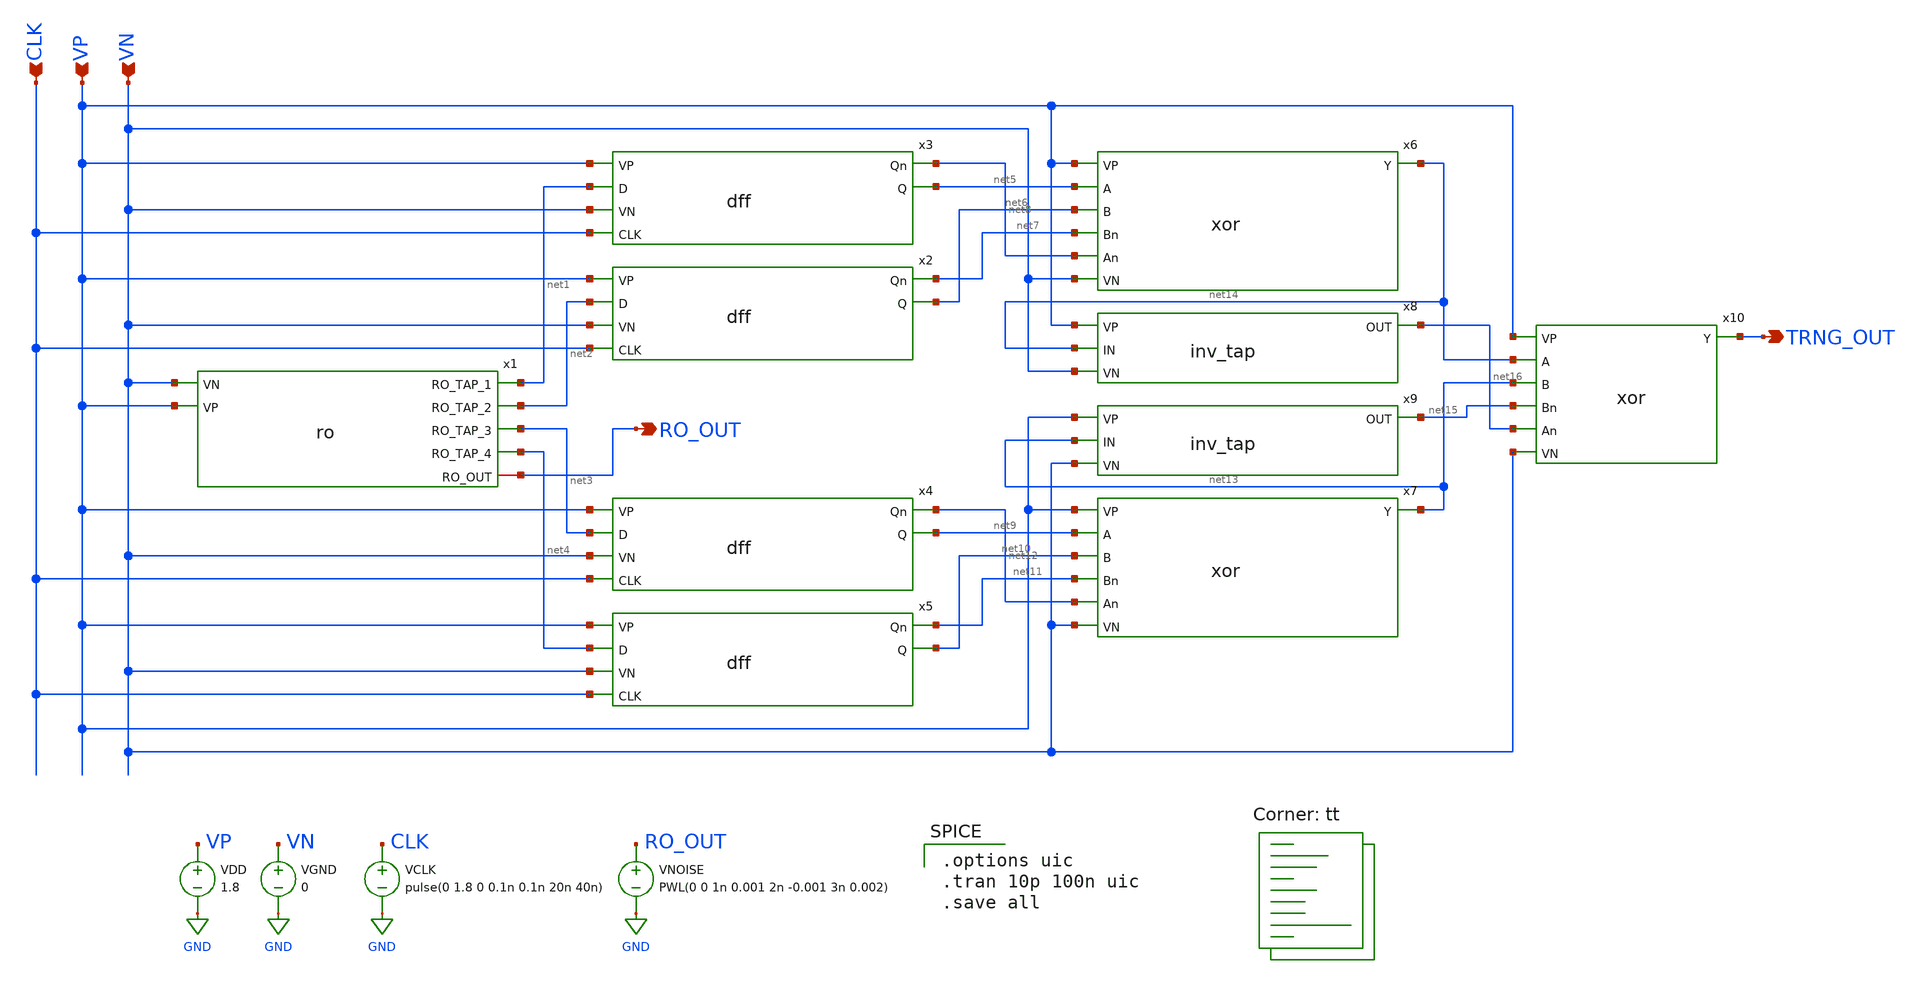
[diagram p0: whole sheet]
** sch_path: Mixed-Signal TRNG/xschem/trng.sch
**.subckt trng VP VN TRNG_OUT CLK RO_OUT
*.ipin VP
*.ipin VN
*.opin TRNG_OUT
*.ipin CLK
*.opin RO_OUT
x2 VP net7 net2 net6 VN CLK dff
x3 VP net8 net1 net5 VN CLK dff
x4 VP net12 net3 net9 VN CLK dff
x5 VP net11 net4 net10 VN CLK dff
x6 VP net5 net6 net14 net7 net8 VN xor
x7 VP net9 net10 net13 net11 net12 VN xor
x8 VP net14 net16 VN inv_tap
x9 VP net13 net15 VN inv_tap
x10 VP net14 net13 TRNG_OUT net15 net16 VN xor
VDD VP GND 1.8
VGND VN GND 0
VCLK CLK GND pulse(0 1.8 0 0.1n 0.1n 20n 40n)
x1 net1 net2 net3 net4 RO_OUT VN VP ro
VNOISE RO_OUT GND PWL(0 0 1n 0.001 2n -0.001 3n 0.002)
**** begin user architecture code

.options uic
.tran 10p 100n uic
.save all

.lib $::SKYWATER_MODELS/sky130.lib.spice tt
**** end user architecture code
**.ends

* expanding   symbol:  /home/madvlsi/Desktop/Mixed-Signal TRNG/xschem/dff.sym # of pins=6
** sym_path: Mixed-Signal TRNG/xschem/dff.sym
** sch_path: Mixed-Signal TRNG/xschem/dff.sch
.subckt dff VP Qn D Q VN CLK
*.opin Qn
*.opin Q
*.ipin D
*.ipin CLK
*.ipin VP
*.ipin VN
XM1 net1 Dn1 VP VP sky130_fd_pr__pfet_01v8 L=0.15 W=2 nf=1 ad='int((nf+1)/2) * W/nf * 0.29' as='int((nf+2)/2) * W/nf * 0.29'
+ pd='2*int((nf+1)/2) * (W/nf + 0.29)' ps='2*int((nf+2)/2) * (W/nf + 0.29)' nrd='0.29 / W' nrs='0.29 / W'
+ sa=0 sb=0 sd=0 mult=1 m=1
XM2 net1 CLK VP VP sky130_fd_pr__pfet_01v8 L=0.15 W=4 nf=1 ad='int((nf+1)/2) * W/nf * 0.29' as='int((nf+2)/2) * W/nf * 0.29'
+ pd='2*int((nf+1)/2) * (W/nf + 0.29)' ps='2*int((nf+2)/2) * (W/nf + 0.29)' nrd='0.29 / W' nrs='0.29 / W'
+ sa=0 sb=0 sd=0 mult=1 m=1
XM3 net7 net10 net1 VP sky130_fd_pr__pfet_01v8 L=0.15 W=2 nf=1 ad='int((nf+1)/2) * W/nf * 0.29' as='int((nf+2)/2) * W/nf * 0.29'
+ pd='2*int((nf+1)/2) * (W/nf + 0.29)' ps='2*int((nf+2)/2) * (W/nf + 0.29)' nrd='0.29 / W' nrs='0.29 / W'
+ sa=0 sb=0 sd=0 mult=1 m=1
XM4 VP D net2 VP sky130_fd_pr__pfet_01v8 L=0.15 W=2 nf=1 ad='int((nf+1)/2) * W/nf * 0.29' as='int((nf+2)/2) * W/nf * 0.29'
+ pd='2*int((nf+1)/2) * (W/nf + 0.29)' ps='2*int((nf+2)/2) * (W/nf + 0.29)' nrd='0.29 / W' nrs='0.29 / W'
+ sa=0 sb=0 sd=0 mult=1 m=1
XM5 net2 CLK VP VP sky130_fd_pr__pfet_01v8 L=0.15 W=4 nf=1 ad='int((nf+1)/2) * W/nf * 0.29' as='int((nf+2)/2) * W/nf * 0.29'
+ pd='2*int((nf+1)/2) * (W/nf + 0.29)' ps='2*int((nf+2)/2) * (W/nf + 0.29)' nrd='0.29 / W' nrs='0.29 / W'
+ sa=0 sb=0 sd=0 mult=1 m=1
XM6 net10 net7 net2 VP sky130_fd_pr__pfet_01v8 L=0.15 W=2 nf=1 ad='int((nf+1)/2) * W/nf * 0.29' as='int((nf+2)/2) * W/nf * 0.29'
+ pd='2*int((nf+1)/2) * (W/nf + 0.29)' ps='2*int((nf+2)/2) * (W/nf + 0.29)' nrd='0.29 / W' nrs='0.29 / W'
+ sa=0 sb=0 sd=0 mult=1 m=1
XM7 VP net7 net3 VP sky130_fd_pr__pfet_01v8 L=0.15 W=2 nf=1 ad='int((nf+1)/2) * W/nf * 0.29' as='int((nf+2)/2) * W/nf * 0.29'
+ pd='2*int((nf+1)/2) * (W/nf + 0.29)' ps='2*int((nf+2)/2) * (W/nf + 0.29)' nrd='0.29 / W' nrs='0.29 / W'
+ sa=0 sb=0 sd=0 mult=1 m=1
XM8 Qn CLK net3 VP sky130_fd_pr__pfet_01v8 L=0.15 W=4 nf=1 ad='int((nf+1)/2) * W/nf * 0.29' as='int((nf+2)/2) * W/nf * 0.29'
+ pd='2*int((nf+1)/2) * (W/nf + 0.29)' ps='2*int((nf+2)/2) * (W/nf + 0.29)' nrd='0.29 / W' nrs='0.29 / W'
+ sa=0 sb=0 sd=0 mult=1 m=1
XM9 VP Q Qn VP sky130_fd_pr__pfet_01v8 L=0.15 W=4 nf=1 ad='int((nf+1)/2) * W/nf * 0.29' as='int((nf+2)/2) * W/nf * 0.29'
+ pd='2*int((nf+1)/2) * (W/nf + 0.29)' ps='2*int((nf+2)/2) * (W/nf + 0.29)' nrd='0.29 / W' nrs='0.29 / W'
+ sa=0 sb=0 sd=0 mult=1 m=1
XM10 net4 net10 VP VP sky130_fd_pr__pfet_01v8 L=0.15 W=2 nf=1 ad='int((nf+1)/2) * W/nf * 0.29' as='int((nf+2)/2) * W/nf * 0.29'
+ pd='2*int((nf+1)/2) * (W/nf + 0.29)' ps='2*int((nf+2)/2) * (W/nf + 0.29)' nrd='0.29 / W' nrs='0.29 / W'
+ sa=0 sb=0 sd=0 mult=1 m=1
XM11 Q CLK net4 VP sky130_fd_pr__pfet_01v8 L=0.15 W=4 nf=1 ad='int((nf+1)/2) * W/nf * 0.29' as='int((nf+2)/2) * W/nf * 0.29'
+ pd='2*int((nf+1)/2) * (W/nf + 0.29)' ps='2*int((nf+2)/2) * (W/nf + 0.29)' nrd='0.29 / W' nrs='0.29 / W'
+ sa=0 sb=0 sd=0 mult=1 m=1
XM12 VP Qn Q VP sky130_fd_pr__pfet_01v8 L=0.15 W=4 nf=1 ad='int((nf+1)/2) * W/nf * 0.29' as='int((nf+2)/2) * W/nf * 0.29'
+ pd='2*int((nf+1)/2) * (W/nf + 0.29)' ps='2*int((nf+2)/2) * (W/nf + 0.29)' nrd='0.29 / W' nrs='0.29 / W'
+ sa=0 sb=0 sd=0 mult=1 m=1
XM13 net9 D VN VN sky130_fd_pr__nfet_01v8 L=0.15 W=1 nf=1 ad='int((nf+1)/2) * W/nf * 0.29' as='int((nf+2)/2) * W/nf * 0.29'
+ pd='2*int((nf+1)/2) * (W/nf + 0.29)' ps='2*int((nf+2)/2) * (W/nf + 0.29)' nrd='0.29 / W' nrs='0.29 / W'
+ sa=0 sb=0 sd=0 mult=1 m=1
XM14 net9 CLK net10 VN sky130_fd_pr__nfet_01v8 L=0.15 W=2 nf=1 ad='int((nf+1)/2) * W/nf * 0.29' as='int((nf+2)/2) * W/nf * 0.29'
+ pd='2*int((nf+1)/2) * (W/nf + 0.29)' ps='2*int((nf+2)/2) * (W/nf + 0.29)' nrd='0.29 / W' nrs='0.29 / W'
+ sa=0 sb=0 sd=0 mult=1 m=1
XM15 VN net7 net10 VN sky130_fd_pr__nfet_01v8 L=0.15 W=1 nf=1 ad='int((nf+1)/2) * W/nf * 0.29' as='int((nf+2)/2) * W/nf * 0.29'
+ pd='2*int((nf+1)/2) * (W/nf + 0.29)' ps='2*int((nf+2)/2) * (W/nf + 0.29)' nrd='0.29 / W' nrs='0.29 / W'
+ sa=0 sb=0 sd=0 mult=1 m=1
XM16 VN net10 net5 VN sky130_fd_pr__nfet_01v8 L=0.15 W=1 nf=1 ad='int((nf+1)/2) * W/nf * 0.29' as='int((nf+2)/2) * W/nf * 0.29'
+ pd='2*int((nf+1)/2) * (W/nf + 0.29)' ps='2*int((nf+2)/2) * (W/nf + 0.29)' nrd='0.29 / W' nrs='0.29 / W'
+ sa=0 sb=0 sd=0 mult=1 m=1
XM17 VN CLK net5 VN sky130_fd_pr__nfet_01v8 L=0.15 W=2 nf=1 ad='int((nf+1)/2) * W/nf * 0.29' as='int((nf+2)/2) * W/nf * 0.29'
+ pd='2*int((nf+1)/2) * (W/nf + 0.29)' ps='2*int((nf+2)/2) * (W/nf + 0.29)' nrd='0.29 / W' nrs='0.29 / W'
+ sa=0 sb=0 sd=0 mult=1 m=1
XM18 Q Qn net5 VN sky130_fd_pr__nfet_01v8 L=0.15 W=2 nf=1 ad='int((nf+1)/2) * W/nf * 0.29' as='int((nf+2)/2) * W/nf * 0.29'
+ pd='2*int((nf+1)/2) * (W/nf + 0.29)' ps='2*int((nf+2)/2) * (W/nf + 0.29)' nrd='0.29 / W' nrs='0.29 / W'
+ sa=0 sb=0 sd=0 mult=1 m=1
XM19 VN Dn2 net8 VN sky130_fd_pr__nfet_01v8 L=0.15 W=1 nf=1 ad='int((nf+1)/2) * W/nf * 0.29' as='int((nf+2)/2) * W/nf * 0.29'
+ pd='2*int((nf+1)/2) * (W/nf + 0.29)' ps='2*int((nf+2)/2) * (W/nf + 0.29)' nrd='0.29 / W' nrs='0.29 / W'
+ sa=0 sb=0 sd=0 mult=1 m=1
XM20 net8 CLK net7 VN sky130_fd_pr__nfet_01v8 L=0.15 W=2 nf=1 ad='int((nf+1)/2) * W/nf * 0.29' as='int((nf+2)/2) * W/nf * 0.29'
+ pd='2*int((nf+1)/2) * (W/nf + 0.29)' ps='2*int((nf+2)/2) * (W/nf + 0.29)' nrd='0.29 / W' nrs='0.29 / W'
+ sa=0 sb=0 sd=0 mult=1 m=1
XM21 VN net10 net7 VN sky130_fd_pr__nfet_01v8 L=0.15 W=1 nf=1 ad='int((nf+1)/2) * W/nf * 0.29' as='int((nf+2)/2) * W/nf * 0.29'
+ pd='2*int((nf+1)/2) * (W/nf + 0.29)' ps='2*int((nf+2)/2) * (W/nf + 0.29)' nrd='0.29 / W' nrs='0.29 / W'
+ sa=0 sb=0 sd=0 mult=1 m=1
XM22 net6 net7 VN VN sky130_fd_pr__nfet_01v8 L=0.15 W=1 nf=1 ad='int((nf+1)/2) * W/nf * 0.29' as='int((nf+2)/2) * W/nf * 0.29'
+ pd='2*int((nf+1)/2) * (W/nf + 0.29)' ps='2*int((nf+2)/2) * (W/nf + 0.29)' nrd='0.29 / W' nrs='0.29 / W'
+ sa=0 sb=0 sd=0 mult=1 m=1
XM23 VN CLK net6 VN sky130_fd_pr__nfet_01v8 L=0.15 W=2 nf=1 ad='int((nf+1)/2) * W/nf * 0.29' as='int((nf+2)/2) * W/nf * 0.29'
+ pd='2*int((nf+1)/2) * (W/nf + 0.29)' ps='2*int((nf+2)/2) * (W/nf + 0.29)' nrd='0.29 / W' nrs='0.29 / W'
+ sa=0 sb=0 sd=0 mult=1 m=1
XM24 Qn Q net6 VN sky130_fd_pr__nfet_01v8 L=0.15 W=2 nf=1 ad='int((nf+1)/2) * W/nf * 0.29' as='int((nf+2)/2) * W/nf * 0.29'
+ pd='2*int((nf+1)/2) * (W/nf + 0.29)' ps='2*int((nf+2)/2) * (W/nf + 0.29)' nrd='0.29 / W' nrs='0.29 / W'
+ sa=0 sb=0 sd=0 mult=1 m=1
VDD VP GND 1.8
VGND VN GND 0
VCLK CLK GND pulse(0 1.8 0 0.1n 0.1n 10n 20n)
VD D GND pulse(0 1.8 0 0.1n 0.1n 40n 80n)
V_Dn1 Dn1 GND pulse(1.8 0 0 0.1n 0.1n 10n 20n)
V_Dn2 Dn2 GND pulse(0 1.8 0 0.1n 0.1n 10n 20n)
**** begin user architecture code
.lib $::SKYWATER_MODELS/sky130.lib.spice tt
**** end user architecture code
**** begin user architecture code

.tran 0.1n 400n
.save all

**** end user architecture code
.ends


* expanding   symbol:  /home/madvlsi/Desktop/Mixed-Signal TRNG/xschem/xor.sym # of pins=7
** sym_path: Mixed-Signal TRNG/xschem/xor.sym
** sch_path: Mixed-Signal TRNG/xschem/xor.sch
.subckt xor VP A B Y Bn An VN
*.ipin B
*.ipin Bn
*.ipin A
*.ipin An
*.opin Y
*.ipin VP
*.ipin VN
XM3 net1 Bn An VP sky130_fd_pr__pfet_01v8 L=0.15 W=4 nf=1 ad='int((nf+1)/2) * W/nf * 0.29' as='int((nf+2)/2) * W/nf * 0.29'
+ pd='2*int((nf+1)/2) * (W/nf + 0.29)' ps='2*int((nf+2)/2) * (W/nf + 0.29)' nrd='0.29 / W' nrs='0.29 / W'
+ sa=0 sb=0 sd=0 mult=1 m=1
XM4 net1 B An VN sky130_fd_pr__nfet_01v8 L=0.15 W=2 nf=1 ad='int((nf+1)/2) * W/nf * 0.29' as='int((nf+2)/2) * W/nf * 0.29'
+ pd='2*int((nf+1)/2) * (W/nf + 0.29)' ps='2*int((nf+2)/2) * (W/nf + 0.29)' nrd='0.29 / W' nrs='0.29 / W'
+ sa=0 sb=0 sd=0 mult=1 m=1
XM5 net2 net1 VP VP sky130_fd_pr__pfet_01v8 L=0.15 W=4 nf=1 ad='int((nf+1)/2) * W/nf * 0.29' as='int((nf+2)/2) * W/nf * 0.29'
+ pd='2*int((nf+1)/2) * (W/nf + 0.29)' ps='2*int((nf+2)/2) * (W/nf + 0.29)' nrd='0.29 / W' nrs='0.29 / W'
+ sa=0 sb=0 sd=0 mult=1 m=1
XM6 net2 net1 VN VN sky130_fd_pr__nfet_01v8 L=0.15 W=2 nf=1 ad='int((nf+1)/2) * W/nf * 0.29' as='int((nf+2)/2) * W/nf * 0.29'
+ pd='2*int((nf+1)/2) * (W/nf + 0.29)' ps='2*int((nf+2)/2) * (W/nf + 0.29)' nrd='0.29 / W' nrs='0.29 / W'
+ sa=0 sb=0 sd=0 mult=1 m=1
XM1 net1 B A VP sky130_fd_pr__pfet_01v8 L=0.15 W=4 nf=1 ad='int((nf+1)/2) * W/nf * 0.29' as='int((nf+2)/2) * W/nf * 0.29'
+ pd='2*int((nf+1)/2) * (W/nf + 0.29)' ps='2*int((nf+2)/2) * (W/nf + 0.29)' nrd='0.29 / W' nrs='0.29 / W'
+ sa=0 sb=0 sd=0 mult=1 m=1
XM2 net1 Bn A VN sky130_fd_pr__nfet_01v8 L=0.15 W=2 nf=1 ad='int((nf+1)/2) * W/nf * 0.29' as='int((nf+2)/2) * W/nf * 0.29'
+ pd='2*int((nf+1)/2) * (W/nf + 0.29)' ps='2*int((nf+2)/2) * (W/nf + 0.29)' nrd='0.29 / W' nrs='0.29 / W'
+ sa=0 sb=0 sd=0 mult=1 m=1
**** begin user architecture code

.tran 0.05n 60n
.save all

**** end user architecture code
VDD VP GND 1.8
**** begin user architecture code
.lib $::SKYWATER_MODELS/sky130.lib.spice tt
**** end user architecture code
VGND VN GND 0
V_A A GND pulse(0 1.8 0ns 0.1ns 0.1ns 5ns 10n)
V_B B GND pulse(0 1.8 2.5ns 0.1ns 0.1ns 5ns 10n)
V_An An GND pulse(1.8 0 0ns 0.1ns 0.1ns 5ns 10n)
V_Bn Bn GND pulse(1.8 0 2.5ns 0.1ns 0.1ns 5ns 10n)
XM7 Y net2 VP VP sky130_fd_pr__pfet_01v8 L=0.15 W=4 nf=1 ad='int((nf+1)/2) * W/nf * 0.29' as='int((nf+2)/2) * W/nf * 0.29'
+ pd='2*int((nf+1)/2) * (W/nf + 0.29)' ps='2*int((nf+2)/2) * (W/nf + 0.29)' nrd='0.29 / W' nrs='0.29 / W'
+ sa=0 sb=0 sd=0 mult=1 m=1
XM8 Y net2 VN VN sky130_fd_pr__nfet_01v8 L=0.15 W=2 nf=1 ad='int((nf+1)/2) * W/nf * 0.29' as='int((nf+2)/2) * W/nf * 0.29'
+ pd='2*int((nf+1)/2) * (W/nf + 0.29)' ps='2*int((nf+2)/2) * (W/nf + 0.29)' nrd='0.29 / W' nrs='0.29 / W'
+ sa=0 sb=0 sd=0 mult=1 m=1
.ends


* expanding   symbol:  /home/madvlsi/Desktop/Mixed-Signal TRNG/xschem/inv_tap.sym # of pins=4
** sym_path: Mixed-Signal TRNG/xschem/inv_tap.sym
** sch_path: Mixed-Signal TRNG/xschem/inv_tap.sch
.subckt inv_tap VP IN OUT VN
*.ipin IN
*.opin OUT
*.ipin VP
*.ipin VN
XM1 OUT IN VN VN sky130_fd_pr__nfet_01v8 L=0.15 W=0.6 nf=1 ad='int((nf+1)/2) * W/nf * 0.29' as='int((nf+2)/2) * W/nf * 0.29'
+ pd='2*int((nf+1)/2) * (W/nf + 0.29)' ps='2*int((nf+2)/2) * (W/nf + 0.29)' nrd='0.29 / W' nrs='0.29 / W'
+ sa=0 sb=0 sd=0 mult=1 m=1
XM2 OUT IN VP VP sky130_fd_pr__pfet_01v8 L=0.15 W=1.2 nf=1 ad='int((nf+1)/2) * W/nf * 0.29' as='int((nf+2)/2) * W/nf * 0.29'
+ pd='2*int((nf+1)/2) * (W/nf + 0.29)' ps='2*int((nf+2)/2) * (W/nf + 0.29)' nrd='0.29 / W' nrs='0.29 / W'
+ sa=0 sb=0 sd=0 mult=1 m=1
.ends


* expanding   symbol:  /home/madvlsi/Desktop/Mixed-Signal TRNG/xschem/ro.sym # of pins=7
** sym_path: Mixed-Signal TRNG/xschem/ro.sym
** sch_path: Mixed-Signal TRNG/xschem/ro.sch
.subckt ro RO_TAP_1 RO_TAP_2 RO_TAP_3 RO_TAP_4 RO_OUT VN VP
*.iopin RO_OUT
*.ipin VP
*.ipin VN
*.opin RO_TAP_1
*.opin RO_TAP_2
*.opin RO_TAP_3
*.opin RO_TAP_4
x1 VP RO_OUT net1 VN inv
x2 VP net1 net2 VN inv
x3 VP net2 net3 VN inv
x4 VP net3 net4 VN inv
x5 VP net4 RO_OUT VN inv
**** begin user architecture code

.tran 0.01n 10n
.save all

**** end user architecture code
VDD VP GND 1.8
**** begin user architecture code
.lib $::SKYWATER_MODELS/sky130.lib.spice tt
**** end user architecture code
VGND VN GND 0
x6 VP net1 RO_TAP_1 VN inv_tap
x7 VP net2 RO_TAP_2 VN inv_tap
x8 VP net3 RO_TAP_3 VN inv_tap
x9 VP net4 RO_TAP_4 VN inv_tap
.ends


* expanding   symbol:  /home/madvlsi/Desktop/Mixed-Signal TRNG/xschem/inv.sym # of pins=4
** sym_path: Mixed-Signal TRNG/xschem/inv.sym
** sch_path: Mixed-Signal TRNG/xschem/inv.sch
.subckt inv VP IN OUT VN
*.ipin IN
*.opin OUT
*.ipin VP
*.ipin VN
XM1 OUT IN VN VN sky130_fd_pr__nfet_01v8 L=0.15 W=2 nf=1 ad='int((nf+1)/2) * W/nf * 0.29' as='int((nf+2)/2) * W/nf * 0.29'
+ pd='2*int((nf+1)/2) * (W/nf + 0.29)' ps='2*int((nf+2)/2) * (W/nf + 0.29)' nrd='0.29 / W' nrs='0.29 / W'
+ sa=0 sb=0 sd=0 mult=1 m=1
XM2 OUT IN VP VP sky130_fd_pr__pfet_01v8 L=0.15 W=4 nf=1 ad='int((nf+1)/2) * W/nf * 0.29' as='int((nf+2)/2) * W/nf * 0.29'
+ pd='2*int((nf+1)/2) * (W/nf + 0.29)' ps='2*int((nf+2)/2) * (W/nf + 0.29)' nrd='0.29 / W' nrs='0.29 / W'
+ sa=0 sb=0 sd=0 mult=1 m=1
.ends

.GLOBAL GND
.end
